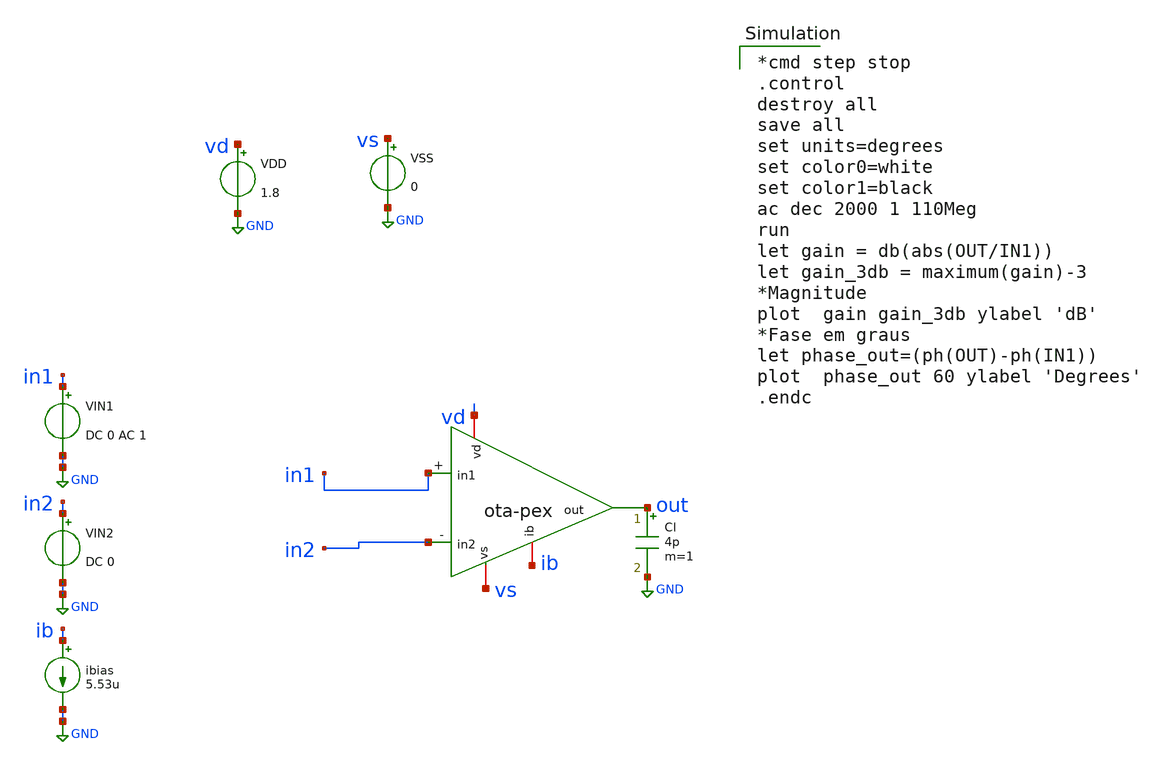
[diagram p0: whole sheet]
** sch_path: ota/xschem/ota_tb-ac.sch
* Copyright 2020 Stefan Frederik Schippers
* Licensed under the Apache License, Version 2.0 (the "License");
* you may not use this file except in compliance with the License.
* You may obtain a copy of the License at
* https://www.apache.org/licenses/LICENSE-2.0
* Unless required by applicable law or agreed to in writing, software
* distributed under the License is distributed on an "AS IS" BASIS,
* WITHOUT WARRANTIES OR CONDITIONS OF ANY KIND, either express or implied.
* See the License for the specific language governing permissions and
* limitations under the License.
**.subckt ota_tb-ac
VIN1 in1 GND DC 0 AC 1
ibias ib GND 5.53u
VDD vd GND 1.8
VSS vs GND 0
VIN2 in2 GND DC 0
Cl out GND 4p m=1
X1 vd ib out in2 in1 vs ota-pex
**** begin user architecture code

*cmd step stop
.control
destroy all
save all
set units=degrees
set color0=white
set color1=black
ac dec 2000 1 110Meg
run
let gain = db(abs(OUT/IN1))
let gain_3db = maximum(gain)-3
*Magnitude
plot  gain gain_3db ylabel 'dB'
*Fase em graus
let phase_out=(ph(OUT)-ph(IN1))
plot  phase_out 60 ylabel 'Degrees'
.endc

 .lib $::SKYWATER_MODELS/sky130.lib.spice tt
.include $::SKYWATER_STDCELLS/sky130_fd_sc_hd.spice

**** end user architecture code
**.ends
.GLOBAL GND
.end
